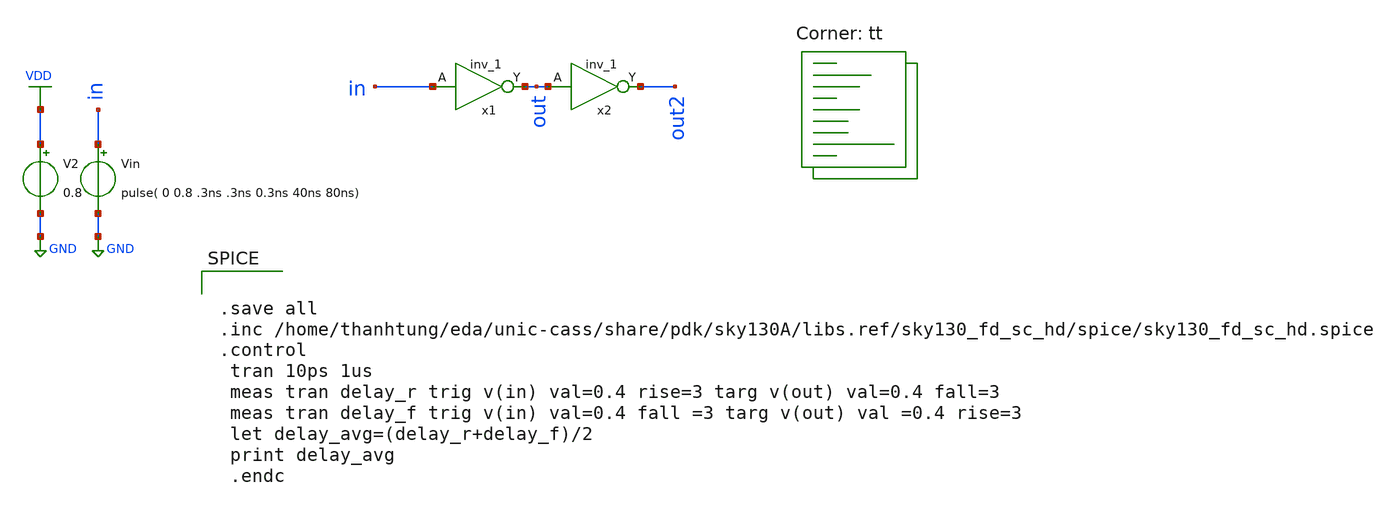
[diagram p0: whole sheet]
** sch_path: d_inver_fan.sch
**.subckt d_inver_fan
x1 in GND GND VDD VDD out sky130_fd_sc_hd__inv_1
V2 VDD GND 0.8
Vin in GND pulse( 0 0.8 .3ns .3ns 0.3ns 40ns 80ns)
x2 out GND GND VDD VDD out2 sky130_fd_sc_hd__inv_1
**** begin user architecture code
.lib $::SKYWATER_MODELS/sky130.lib.spice tt


.save all
.inc /home/thanhtung/eda/unic-cass/share/pdk/sky130A/libs.ref/sky130_fd_sc_hd/spice/sky130_fd_sc_hd.spice
.control
 tran 10ps 1us
 meas tran delay_r trig v(in) val=0.4 rise=3 targ v(out) val=0.4 fall=3
 meas tran delay_f trig v(in) val=0.4 fall =3 targ v(out) val =0.4 rise=3
 let delay_avg=(delay_r+delay_f)/2
 print delay_avg
 .endc


**** end user architecture code
**.ends
.GLOBAL GND
.GLOBAL VDD
.end
